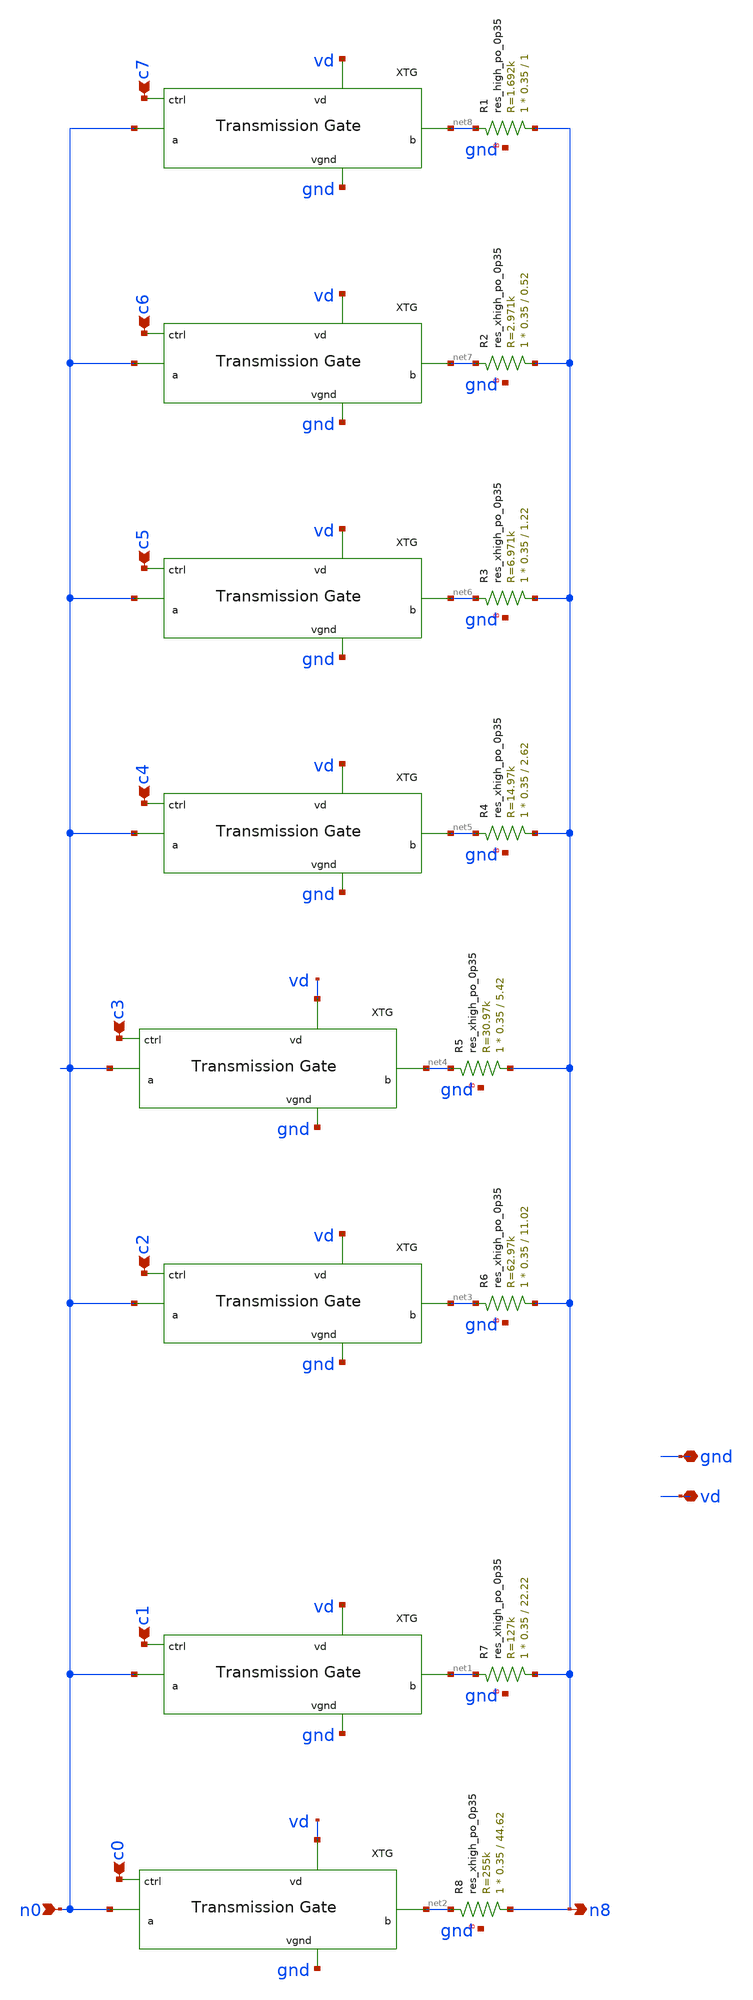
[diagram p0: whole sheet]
** sch_path: xschem/digpotp.sch
**.subckt digpotp gnd vd c0 c1 n0 n8 c2 c3 c4 c5 c6 c7
*.iopin gnd
*.iopin vd
*.ipin c0
*.ipin c1
*.ipin n0
*.opin n8
*.ipin c2
*.ipin c3
*.ipin c4
*.ipin c5
*.ipin c6
*.ipin c7
x9 c0 vd net2 gnd n0 tg
x10 c1 vd net1 gnd n0 tg
x7 c2 vd net3 gnd n0 tg
x8 c3 vd net4 gnd n0 tg
x11 c4 vd net5 gnd n0 tg
x12 c5 vd net6 gnd n0 tg
x1 c6 vd net7 gnd n0 tg
x2 c7 vd net8 gnd n0 tg
XR2 n8 net7 gnd sky130_fd_pr__res_xhigh_po_0p35 L=0.52 mult=1 m=1
XR3 n8 net6 gnd sky130_fd_pr__res_xhigh_po_0p35 L=1.22 mult=1 m=1
XR4 n8 net5 gnd sky130_fd_pr__res_xhigh_po_0p35 L=2.62 mult=1 m=1
XR5 n8 net4 gnd sky130_fd_pr__res_xhigh_po_0p35 L=5.42 mult=1 m=1
XR6 n8 net3 gnd sky130_fd_pr__res_xhigh_po_0p35 L=11.02 mult=1 m=1
XR7 n8 net1 gnd sky130_fd_pr__res_xhigh_po_0p35 L=22.22 mult=1 m=1
XR8 n8 net2 gnd sky130_fd_pr__res_xhigh_po_0p35 L=44.62 mult=1 m=1
XR1 n8 net8 gnd sky130_fd_pr__res_high_po_0p35 L=1 mult=1 m=1
**.ends

* expanding   symbol:  projects/dpga-ieee-sscs-contest/xschem/tg.sym # of pins=5
** sym_path: projects/dpga-ieee-sscs-contest/xschem/tg.sym
** sch_path: projects/dpga-ieee-sscs-contest/xschem/tg.sch
.subckt tg ctrl vd b vgnd a
*.iopin vd
*.iopin vgnd
*.iopin b
*.iopin a
*.ipin ctrl
XM2 b nctrl a vd sky130_fd_pr__pfet_01v8 L=0.15 W=60 nf=12 ad='int((nf+1)/2) * W/nf * 0.29' as='int((nf+2)/2) * W/nf * 0.29'
+ pd='2*int((nf+1)/2) * (W/nf + 0.29)' ps='2*int((nf+2)/2) * (W/nf + 0.29)' nrd='0.29 / W' nrs='0.29 / W'
+ sa=0 sb=0 sd=0 mult=1 m=1
XM1 a ctrl b vgnd sky130_fd_pr__nfet_01v8 L=0.15 W=60 nf=12 ad='int((nf+1)/2) * W/nf * 0.29' as='int((nf+2)/2) * W/nf * 0.29'
+ pd='2*int((nf+1)/2) * (W/nf + 0.29)' ps='2*int((nf+2)/2) * (W/nf + 0.29)' nrd='0.29 / W' nrs='0.29 / W'
+ sa=0 sb=0 sd=0 mult=1 m=1
XM3 nctrl ctrl vgnd vgnd sky130_fd_pr__nfet_01v8 L=0.15 W=1 nf=1 ad='int((nf+1)/2) * W/nf * 0.29' as='int((nf+2)/2) * W/nf * 0.29'
+ pd='2*int((nf+1)/2) * (W/nf + 0.29)' ps='2*int((nf+2)/2) * (W/nf + 0.29)' nrd='0.29 / W' nrs='0.29 / W'
+ sa=0 sb=0 sd=0 mult=1 m=1
XM4 nctrl ctrl vd vd sky130_fd_pr__pfet_01v8 L=0.15 W=3 nf=1 ad='int((nf+1)/2) * W/nf * 0.29' as='int((nf+2)/2) * W/nf * 0.29'
+ pd='2*int((nf+1)/2) * (W/nf + 0.29)' ps='2*int((nf+2)/2) * (W/nf + 0.29)' nrd='0.29 / W' nrs='0.29 / W'
+ sa=0 sb=0 sd=0 mult=1 m=1
.ends

.end
